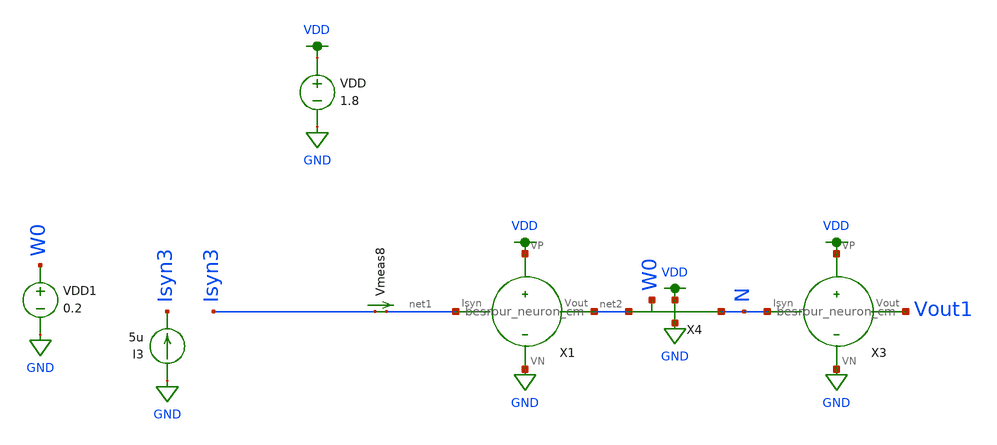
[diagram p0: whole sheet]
** sch_path: schematic/tran_besrour_mem_pls.sch
**.subckt tran_besrour_mem_pls
VDD VDD GND 1.8
VDD1 W0 GND 0.2
I3 GND Isyn3 5u
Vmeas8 Isyn3 net1 0
.save i(vmeas8)
X1 net1 net2 VDD GND besrour_neuron_cm
X3 N Vout1 VDD GND besrour_neuron_cm
X4 VDD GND N net2 W0 memristor_emulator_res
**** begin user architecture code

.param W=2
.param L=0.3
.include ~/neuromorphic_computing_final/schematic/memristor_emulator_res.spice
.include ~/neuromorphic_computing_final/schematic/neuron_top.spice
.tran 1ns 1000us
.save all


.option wnflag=1
.param MC_SWITCH=0.0
.lib ~/skywater/skywater-pdk/libraries/sky130_fd_pr_ngspice/latest/models/sky130.lib.spice tt

**** end user architecture code
**.ends

* expanding   symbol:  /home/madvlsi/neuromorphic_computing_final/schematic/besrour_neuron_cm.sym #
*+ of pins=4
** sym_path: schematic/besrour_neuron_cm.sym
** sch_path: schematic/besrour_neuron_cm.sch
.subckt besrour_neuron_cm Isyn Vout VP VN
*.iopin VP
*.iopin VN
*.iopin Isyn
*.opin Vout
XM2 net2 net1 VP VDD sky130_fd_pr__pfet_01v8 L={L} W={W} nf=1 ad='int((nf+1)/2) * W/nf * 0.29' as='int((nf+2)/2) * W/nf * 0.29'
+ pd='2*int((nf+1)/2) * (W/nf + 0.29)' ps='2*int((nf+2)/2) * (W/nf + 0.29)' nrd='0.29 / W' nrs='0.29 / W'
+ sa=0 sb=0 sd=0 mult=1 m=1
XM3 VP net4 net2 VDD sky130_fd_pr__pfet_01v8 L={L} W={W} nf=1 ad='int((nf+1)/2) * W/nf * 0.29' as='int((nf+2)/2) * W/nf * 0.29'
+ pd='2*int((nf+1)/2) * (W/nf + 0.29)' ps='2*int((nf+2)/2) * (W/nf + 0.29)' nrd='0.29 / W' nrs='0.29 / W'
+ sa=0 sb=0 sd=0 mult=1 m=1
XM4 net4 net2 VP VDD sky130_fd_pr__pfet_01v8 L={L} W={W} nf=1 ad='int((nf+1)/2) * W/nf * 0.29' as='int((nf+2)/2) * W/nf * 0.29'
+ pd='2*int((nf+1)/2) * (W/nf + 0.29)' ps='2*int((nf+2)/2) * (W/nf + 0.29)' nrd='0.29 / W' nrs='0.29 / W'
+ sa=0 sb=0 sd=0 mult=1 m=1
XM5 net3 net4 VP VDD sky130_fd_pr__pfet_01v8 L={L} W={W} nf=1 ad='int((nf+1)/2) * W/nf * 0.29' as='int((nf+2)/2) * W/nf * 0.29'
+ pd='2*int((nf+1)/2) * (W/nf + 0.29)' ps='2*int((nf+2)/2) * (W/nf + 0.29)' nrd='0.29 / W' nrs='0.29 / W'
+ sa=0 sb=0 sd=0 mult=1 m=1
XM6 net4 net2 VN GND sky130_fd_pr__nfet_01v8 L={L} W={W} nf=1 ad='int((nf+1)/2) * W/nf * 0.29' as='int((nf+2)/2) * W/nf * 0.29'
+ pd='2*int((nf+1)/2) * (W/nf + 0.29)' ps='2*int((nf+2)/2) * (W/nf + 0.29)' nrd='0.29 / W' nrs='0.29 / W'
+ sa=0 sb=0 sd=0 mult=1 m=1
XM8 net3 net4 VN GND sky130_fd_pr__nfet_01v8 L={L} W={W} nf=1 ad='int((nf+1)/2) * W/nf * 0.29' as='int((nf+2)/2) * W/nf * 0.29'
+ pd='2*int((nf+1)/2) * (W/nf + 0.29)' ps='2*int((nf+2)/2) * (W/nf + 0.29)' nrd='0.29 / W' nrs='0.29 / W'
+ sa=0 sb=0 sd=0 mult=1 m=1
XM9 net5 net3 VP VDD sky130_fd_pr__pfet_01v8 L={L} W={W} nf=1 ad='int((nf+1)/2) * W/nf * 0.29' as='int((nf+2)/2) * W/nf * 0.29'
+ pd='2*int((nf+1)/2) * (W/nf + 0.29)' ps='2*int((nf+2)/2) * (W/nf + 0.29)' nrd='0.29 / W' nrs='0.29 / W'
+ sa=0 sb=0 sd=0 mult=1 m=1
XM10 net5 net3 VN GND sky130_fd_pr__nfet_01v8 L={L} W={W} nf=1 ad='int((nf+1)/2) * W/nf * 0.29' as='int((nf+2)/2) * W/nf * 0.29'
+ pd='2*int((nf+1)/2) * (W/nf + 0.29)' ps='2*int((nf+2)/2) * (W/nf + 0.29)' nrd='0.29 / W' nrs='0.29 / W'
+ sa=0 sb=0 sd=0 mult=1 m=1
XM11 Vout net5 VP VDD sky130_fd_pr__pfet_01v8 L={L} W={W} nf=1 ad='int((nf+1)/2) * W/nf * 0.29' as='int((nf+2)/2) * W/nf * 0.29'
+ pd='2*int((nf+1)/2) * (W/nf + 0.29)' ps='2*int((nf+2)/2) * (W/nf + 0.29)' nrd='0.29 / W' nrs='0.29 / W'
+ sa=0 sb=0 sd=0 mult=1 m=1
XM12 Vout net5 VN GND sky130_fd_pr__nfet_01v8 L={L} W={W} nf=1 ad='int((nf+1)/2) * W/nf * 0.29' as='int((nf+2)/2) * W/nf * 0.29'
+ pd='2*int((nf+1)/2) * (W/nf + 0.29)' ps='2*int((nf+2)/2) * (W/nf + 0.29)' nrd='0.29 / W' nrs='0.29 / W'
+ sa=0 sb=0 sd=0 mult=1 m=1
XM13 net1 Isyn VN GND sky130_fd_pr__nfet_01v8 L={L} W={W} nf=1 ad='int((nf+1)/2) * W/nf * 0.29' as='int((nf+2)/2) * W/nf * 0.29'
+ pd='2*int((nf+1)/2) * (W/nf + 0.29)' ps='2*int((nf+2)/2) * (W/nf + 0.29)' nrd='0.29 / W' nrs='0.29 / W'
+ sa=0 sb=0 sd=0 mult=1 m=1
XM14 VN Isyn Isyn GND sky130_fd_pr__nfet_01v8 L={L} W={W} nf=1 ad='int((nf+1)/2) * W/nf * 0.29' as='int((nf+2)/2) * W/nf * 0.29'
+ pd='2*int((nf+1)/2) * (W/nf + 0.29)' ps='2*int((nf+2)/2) * (W/nf + 0.29)' nrd='0.29 / W' nrs='0.29 / W'
+ sa=0 sb=0 sd=0 mult=1 m=1
XM1 VP net1 net1 VDD sky130_fd_pr__pfet_01v8 L={L} W={W} nf=1 ad='int((nf+1)/2) * W/nf * 0.29' as='int((nf+2)/2) * W/nf * 0.29'
+ pd='2*int((nf+1)/2) * (W/nf + 0.29)' ps='2*int((nf+2)/2) * (W/nf + 0.29)' nrd='0.29 / W' nrs='0.29 / W'
+ sa=0 sb=0 sd=0 mult=1 m=1
XM7 VN net3 net2 GND sky130_fd_pr__nfet_01v8 L={L} W={W} nf=1 ad='int((nf+1)/2) * W/nf * 0.29' as='int((nf+2)/2) * W/nf * 0.29'
+ pd='2*int((nf+1)/2) * (W/nf + 0.29)' ps='2*int((nf+2)/2) * (W/nf + 0.29)' nrd='0.29 / W' nrs='0.29 / W'
+ sa=0 sb=0 sd=0 mult=1 m=1
XC1 net2 VN sky130_fd_pr__cap_mim_m3_1 W=9.3 L=14 MF=1 m=1
XC2 net3 VN sky130_fd_pr__cap_mim_m3_1 W=9.3 L=14 MF=1 m=1
.ends

.GLOBAL GND
.GLOBAL VDD
.end
